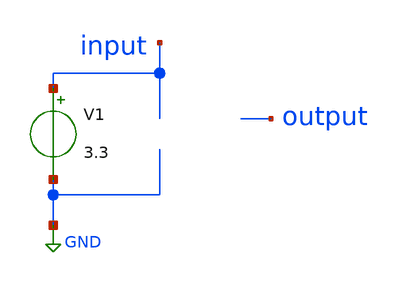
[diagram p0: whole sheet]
** sch_path: voltagedivider_tb.sch
**.subckt voltagedivider_tb
V1 input GND 3.3
**** begin user architecture code


.lib /foss/pdks/sky130A/libs.tech/ngspice/sky130.lib.spice tt
.include voltagedivider.spice

.option wnflag=0
.option savecurrents

.control
  save v(input) v(output)

  * Using your friend's style, but optimized to 40 microseconds
  tran 0.1u 40u

  * Plotting with matching lowercase net names
  plot v(input) v(output) title 'Transient Response'
.endc

**** end user architecture code
**.ends
.GLOBAL GND
.end
